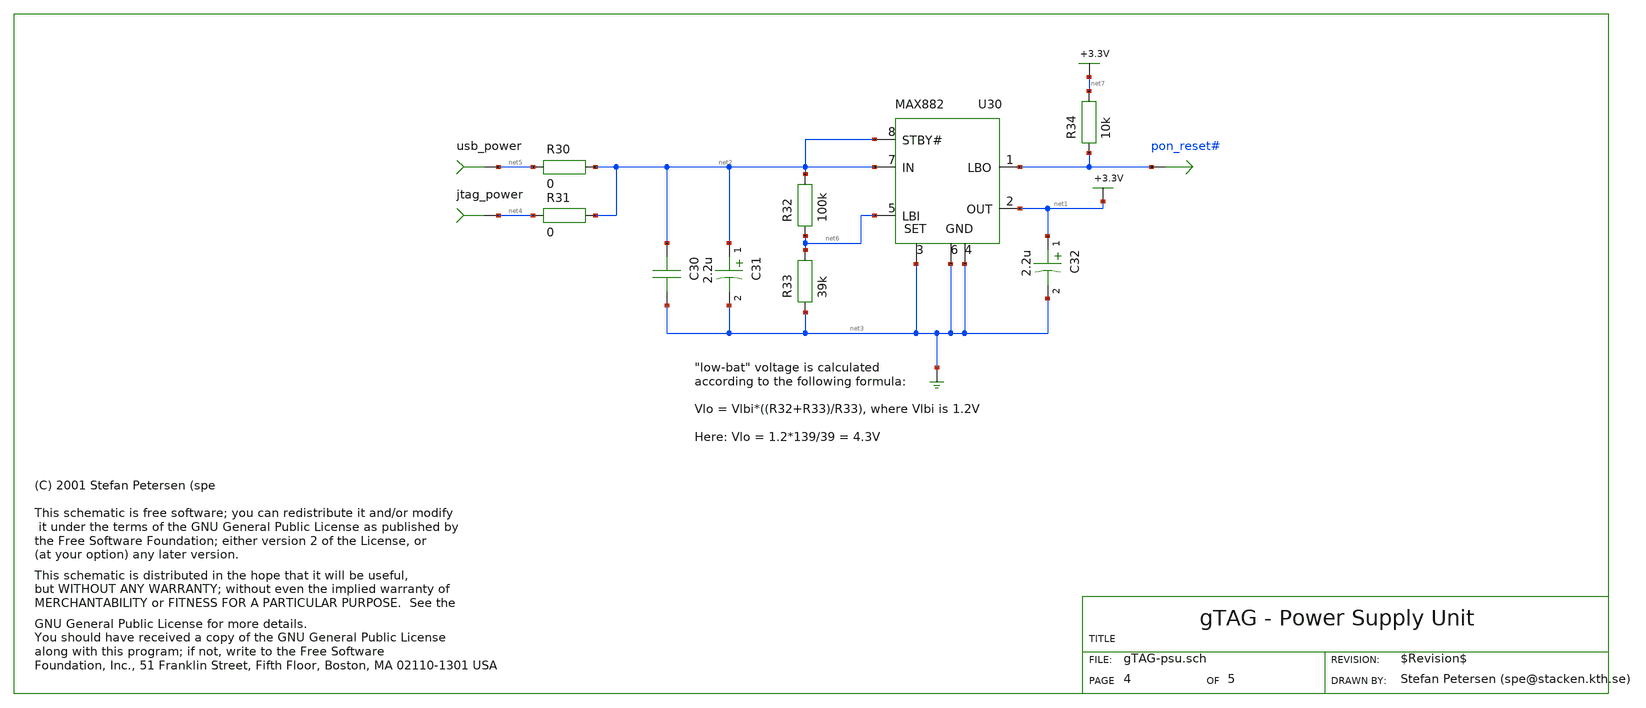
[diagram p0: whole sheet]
** sch_path: xschem_library/gschem_import/gTAG-psu.sch
* copyleft.sym
**.subckt gTAG-psu pon_reset#
usb_power net5
jtag_power net4
U30 net2 net2 net6 net3 net3 net3 net1 pon_reset#
C32 net1 net3 2.2u
C31 net2 net3 2.2u
R30 net5 net2 0
R31 net4 net2 0
C30 net2 net3 100n
C30
R33 net3 net6 39k
R32 net6 net2 100k
R34 pon_reset# net7 10k
**.ends
.end
